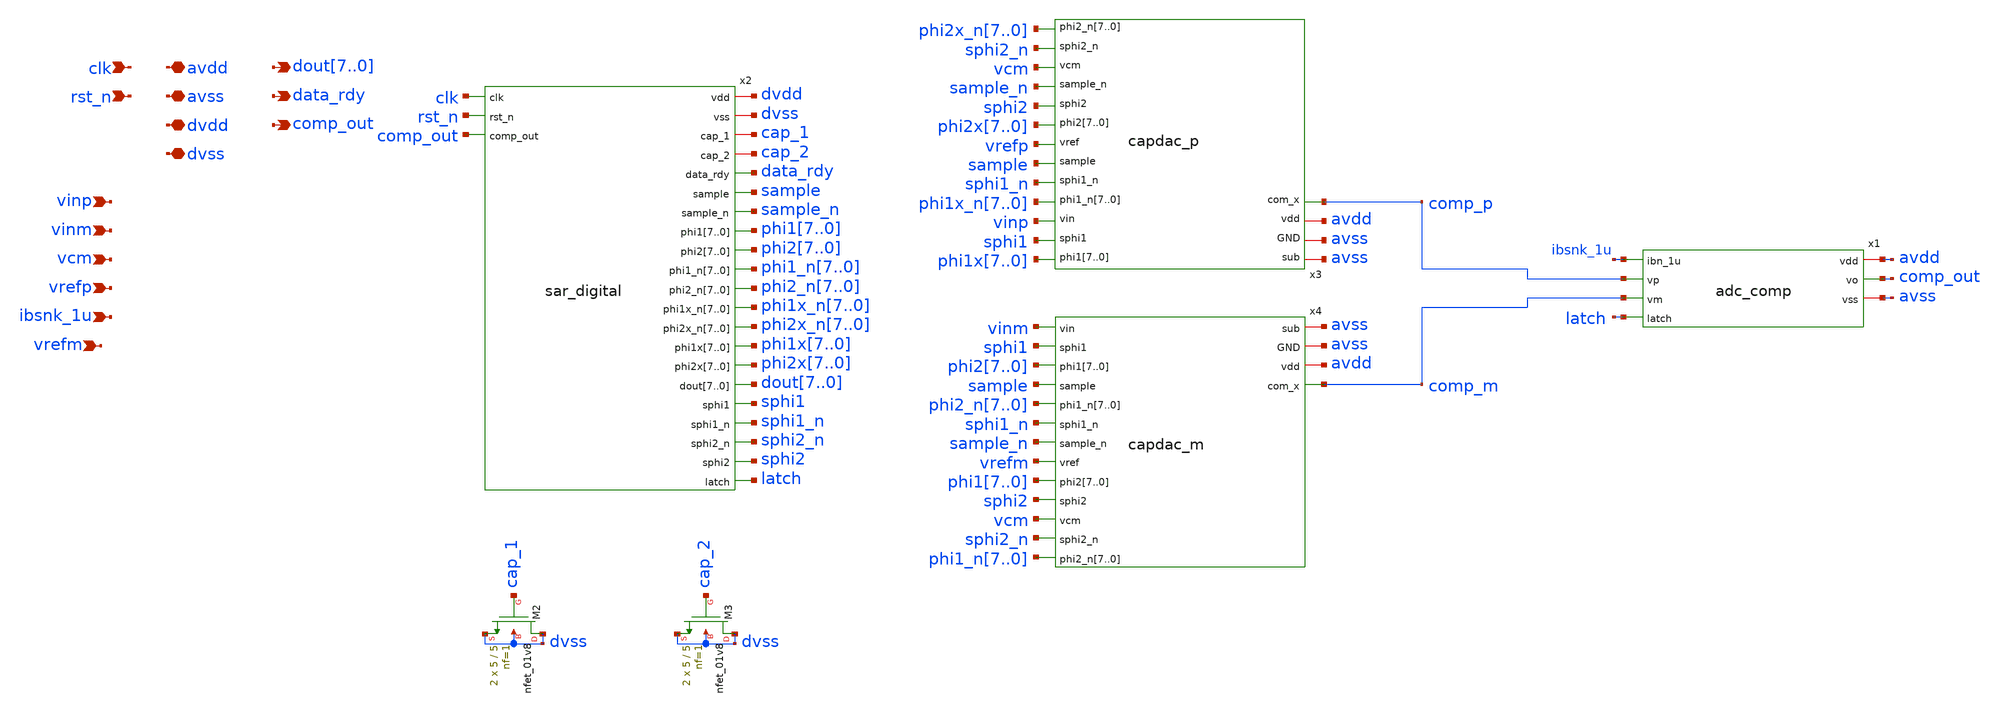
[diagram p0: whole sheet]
** sch_path: top/sar_8bit.sch
**.subckt sar_8bit data_rdy avss avdd clk rst_n dout7,dout6,dout5,dout4,dout3,dout2,dout1,dout0 dvss
*+ dvdd vinp vinm vcm vrefp ibsnk_1u comp_out vrefm
*.opin data_rdy
*.iopin avss
*.iopin avdd
*.ipin clk
*.ipin rst_n
*.opin dout7,dout6,dout5,dout4,dout3,dout2,dout1,dout0
*.iopin dvss
*.iopin dvdd
*.ipin vinp
*.ipin vinm
*.ipin vcm
*.ipin vrefp
*.ipin ibsnk_1u
*.opin comp_out
*.ipin vrefm
x1 avdd comp_out ibsnk_1u comp_p comp_m avss latch adc_comp
XM2 dvss cap_1 dvss dvss sky130_fd_pr__nfet_01v8 L=5 W=5 nf=1 ad='int((nf+1)/2) * W/nf * 0.29' as='int((nf+2)/2) * W/nf * 0.29'
+ pd='2*int((nf+1)/2) * (W/nf + 0.29)' ps='2*int((nf+2)/2) * (W/nf + 0.29)' nrd='0.29 / W' nrs='0.29 / W'
+ sa=0 sb=0 sd=0 mult=2 m=2
XM3 dvss cap_2 dvss dvss sky130_fd_pr__nfet_01v8 L=5 W=5 nf=1 ad='int((nf+1)/2) * W/nf * 0.29' as='int((nf+2)/2) * W/nf * 0.29'
+ pd='2*int((nf+1)/2) * (W/nf + 0.29)' ps='2*int((nf+2)/2) * (W/nf + 0.29)' nrd='0.29 / W' nrs='0.29 / W'
+ sa=0 sb=0 sd=0 mult=2 m=2
x3 phi1x7 phi1x6 phi1x5 phi1x4 phi1x3 phi1x2 phi1x1 phi1x0 sphi1 avss vinp phi1x_n7 phi1x_n6
+ phi1x_n5 phi1x_n4 phi1x_n3 phi1x_n2 phi1x_n1 phi1x_n0 sphi1_n avss sample vrefp phi2x7 phi2x6 phi2x5 phi2x4
+ phi2x3 phi2x2 phi2x1 phi2x0 sphi2 avdd sample_n vcm sphi2_n phi2x_n7 phi2x_n6 phi2x_n5 phi2x_n4 phi2x_n3
+ phi2x_n2 phi2x_n1 phi2x_n0 comp_p capdac_p
x4 vinm sphi1 phi27 phi26 phi25 phi24 phi23 phi22 phi21 phi20 avss sample phi2_n7 phi2_n6 phi2_n5
+ phi2_n4 phi2_n3 phi2_n2 phi2_n1 phi2_n0 sphi1_n sample_n avss vrefm phi17 phi16 phi15 phi14 phi13 phi12
+ phi11 phi10 sphi2 avdd vcm sphi2_n phi1_n7 phi1_n6 phi1_n5 phi1_n4 phi1_n3 phi1_n2 phi1_n1 phi1_n0 comp_m
+ capdac_m
x2 dvdd clk rst_n dvss comp_out cap_1 cap_2 data_rdy sample sample_n phi17 phi16 phi15 phi14 phi13
+ phi12 phi11 phi10 phi27 phi26 phi25 phi24 phi23 phi22 phi21 phi20 phi1_n7 phi1_n6 phi1_n5 phi1_n4 phi1_n3
+ phi1_n2 phi1_n1 phi1_n0 phi2_n7 phi2_n6 phi2_n5 phi2_n4 phi2_n3 phi2_n2 phi2_n1 phi2_n0 phi1x_n7 phi1x_n6
+ phi1x_n5 phi1x_n4 phi1x_n3 phi1x_n2 phi1x_n1 phi1x_n0 phi2x_n7 phi2x_n6 phi2x_n5 phi2x_n4 phi2x_n3 phi2x_n2
+ phi2x_n1 phi2x_n0 phi1x7 phi1x6 phi1x5 phi1x4 phi1x3 phi1x2 phi1x1 phi1x0 phi2x7 phi2x6 phi2x5 phi2x4 phi2x3
+ phi2x2 phi2x1 phi2x0 dout7 dout6 dout5 dout4 dout3 dout2 dout1 dout0 sphi1 sphi1_n sphi2_n sphi2 latch
+ sar_digital
**.ends
.end
